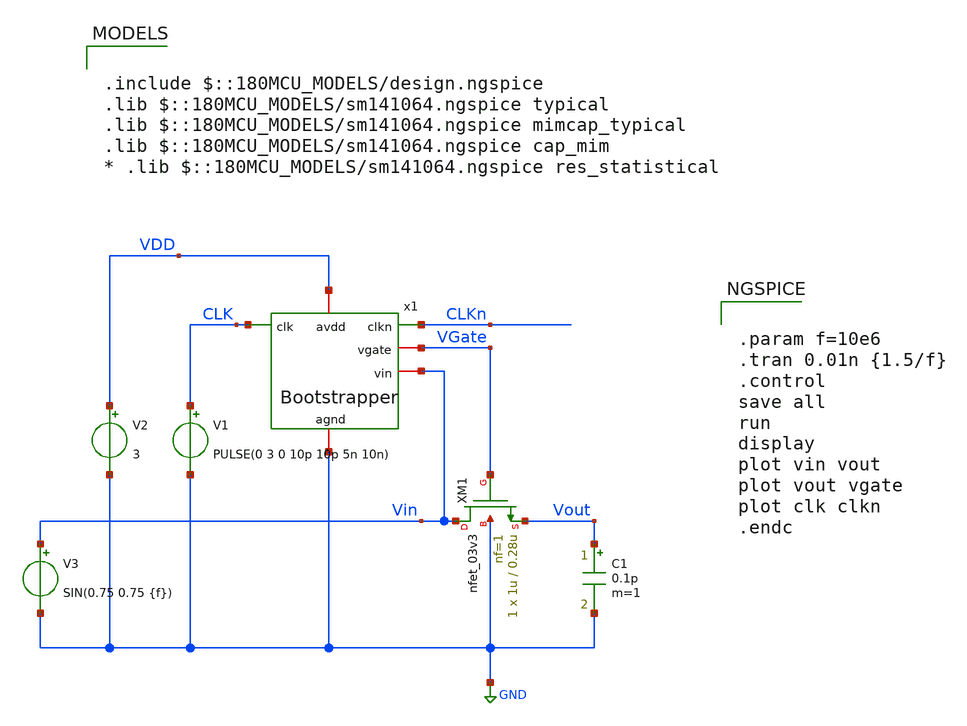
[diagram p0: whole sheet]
** sch_path: mpw18h1/cisar-gen/xschem/Bootstrap_tb.sch
**.subckt Bootstrap_tb
x1 VDD VGate CLK Vin CLKn GND Bootstrapper
XM1 Vin VGate Vout GND nfet_03v3 L=0.28u W=1u nf=1 ad='int((nf+1)/2) * W/nf * 0.18u' as='int((nf+2)/2) * W/nf * 0.18u'
+ pd='2*int((nf+1)/2) * (W/nf + 0.18u)' ps='2*int((nf+2)/2) * (W/nf + 0.18u)' nrd='0.18u / W' nrs='0.18u / W'
+ sa=0 sb=0 sd=0 m=1 par=1
C1 Vout GND 0.1p m=1
V1 CLK GND PULSE(0 3 0 10p 10p 5n 10n)
V2 VDD GND 3
V3 Vin GND SIN(0.75 0.75 {f})
**** begin user architecture code

.include $::180MCU_MODELS/design.ngspice
.lib $::180MCU_MODELS/sm141064.ngspice typical
.lib $::180MCU_MODELS/sm141064.ngspice mimcap_typical
.lib $::180MCU_MODELS/sm141064.ngspice cap_mim
* .lib $::180MCU_MODELS/sm141064.ngspice res_statistical



.param f=10e6
.tran 0.01n {1.5/f}
.control
save all
run
display
plot vin vout
plot vout vgate
plot clk clkn
.endc


**** end user architecture code
**.ends

* expanding   symbol:  SAR_modified/Bootstrapper.sym # of pins=6
** sym_path: mpw18h1/cisar-gen/xschem/Bootstrapper.sym
** sch_path: mpw18h1/cisar-gen/xschem/Bootstrapper.sch
.subckt Bootstrapper avdd vgate clk vin clkn agnd
*.iopin avdd
*.ipin clk
*.iopin vgate
*.iopin agnd
*.iopin vin
*.opin clkn
XM1 avdd vgate C1 avdd pfet_03v3 L=0.28u W=2.4u nf=1 ad='int((nf+1)/2) * W/nf * 0.18u' as='int((nf+2)/2) * W/nf * 0.18u'
+ pd='2*int((nf+1)/2) * (W/nf + 0.18u)' ps='2*int((nf+2)/2) * (W/nf + 0.18u)' nrd='0.18u / W' nrs='0.18u / W'
+ sa=0 sb=0 sd=0 m=1 par=1
XM2 net1 clk avdd avdd pfet_03v3 L=0.28u W=4.8u nf=1 ad='int((nf+1)/2) * W/nf * 0.18u' as='int((nf+2)/2) * W/nf * 0.18u'
+ pd='2*int((nf+1)/2) * (W/nf + 0.18u)' ps='2*int((nf+2)/2) * (W/nf + 0.18u)' nrd='0.18u / W' nrs='0.18u / W'
+ sa=0 sb=0 sd=0 m=1 par=1
XM3 vgate net1 C1 C1 pfet_03v3 L=0.28u W=2.4u nf=1 ad='int((nf+1)/2) * W/nf * 0.18u' as='int((nf+2)/2) * W/nf * 0.18u'
+ pd='2*int((nf+1)/2) * (W/nf + 0.18u)' ps='2*int((nf+2)/2) * (W/nf + 0.18u)' nrd='0.18u / W' nrs='0.18u / W'
+ sa=0 sb=0 sd=0 m=1 par=1
XM4 clkn clk avdd avdd pfet_03v3 L=0.28u W=0.44u nf=1 ad='int((nf+1)/2) * W/nf * 0.18u' as='int((nf+2)/2) * W/nf * 0.18u'
+ pd='2*int((nf+1)/2) * (W/nf + 0.18u)' ps='2*int((nf+2)/2) * (W/nf + 0.18u)' nrd='0.18u / W' nrs='0.18u / W'
+ sa=0 sb=0 sd=0 m=1 par=1
XM5 clkn clk agnd agnd nfet_03v3 L=0.28u W=0.22u nf=1 ad='int((nf+1)/2) * W/nf * 0.18u' as='int((nf+2)/2) * W/nf * 0.18u'
+ pd='2*int((nf+1)/2) * (W/nf + 0.18u)' ps='2*int((nf+2)/2) * (W/nf + 0.18u)' nrd='0.18u / W' nrs='0.18u / W'
+ sa=0 sb=0 sd=0 m=1 par=1
XM6 C2 clkn agnd agnd nfet_03v3 L=0.28u W=2.4u nf=1 ad='int((nf+1)/2) * W/nf * 0.18u' as='int((nf+2)/2) * W/nf * 0.18u'
+ pd='2*int((nf+1)/2) * (W/nf + 0.18u)' ps='2*int((nf+2)/2) * (W/nf + 0.18u)' nrd='0.18u / W' nrs='0.18u / W'
+ sa=0 sb=0 sd=0 m=1 par=1
XM7 net1 clk C2 agnd nfet_03v3 L=0.28u W=2.4u nf=1 ad='int((nf+1)/2) * W/nf * 0.18u' as='int((nf+2)/2) * W/nf * 0.18u'
+ pd='2*int((nf+1)/2) * (W/nf + 0.18u)' ps='2*int((nf+2)/2) * (W/nf + 0.18u)' nrd='0.18u / W' nrs='0.18u / W'
+ sa=0 sb=0 sd=0 m=1 par=1
XM8 C2 vgate net1 agnd nfet_03v3 L=0.28u W=2.4u nf=1 ad='int((nf+1)/2) * W/nf * 0.18u' as='int((nf+2)/2) * W/nf * 0.18u'
+ pd='2*int((nf+1)/2) * (W/nf + 0.18u)' ps='2*int((nf+2)/2) * (W/nf + 0.18u)' nrd='0.18u / W' nrs='0.18u / W'
+ sa=0 sb=0 sd=0 m=1 par=1
XM9 vin vgate C2 agnd nfet_03v3 L=0.28u W=2.4u nf=1 ad='int((nf+1)/2) * W/nf * 0.18u' as='int((nf+2)/2) * W/nf * 0.18u'
+ pd='2*int((nf+1)/2) * (W/nf + 0.18u)' ps='2*int((nf+2)/2) * (W/nf + 0.18u)' nrd='0.18u / W' nrs='0.18u / W'
+ sa=0 sb=0 sd=0 m=1 par=1
XM10 net2 avdd vgate agnd nfet_03v3 L=0.28u W=2.4u nf=1 ad='int((nf+1)/2) * W/nf * 0.18u' as='int((nf+2)/2) * W/nf * 0.18u'
+ pd='2*int((nf+1)/2) * (W/nf + 0.18u)' ps='2*int((nf+2)/2) * (W/nf + 0.18u)' nrd='0.18u / W' nrs='0.18u / W'
+ sa=0 sb=0 sd=0 m=1 par=1
XM11 agnd clkn net2 agnd nfet_03v3 L=0.28u W=2.4u nf=1 ad='int((nf+1)/2) * W/nf * 0.18u' as='int((nf+2)/2) * W/nf * 0.18u'
+ pd='2*int((nf+1)/2) * (W/nf + 0.18u)' ps='2*int((nf+2)/2) * (W/nf + 0.18u)' nrd='0.18u / W' nrs='0.18u / W'
+ sa=0 sb=0 sd=0 m=1 par=1
**** begin user architecture code

* A workaround
XC1 C1 C2 cap_mim_2f0fF c_length=10e-6 c_width=10e-6 m=1


**** end user architecture code
.ends

.GLOBAL GND
.end
